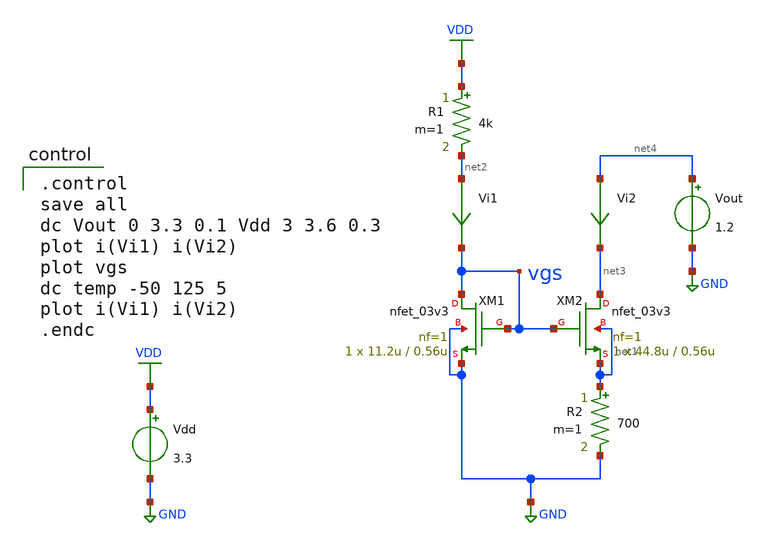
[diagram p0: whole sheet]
** sch_path: current-source/cs-widlar.sch
**.subckt cs-widlar
Vdd VDD GND 3.3
XM1 vgs vgs GND GND nfet_03v3 L=0.56u W=11.2u nf=1 ad='int((nf+1)/2) * W/nf * 0.18u' as='int((nf+2)/2) * W/nf * 0.18u'
+ pd='2*int((nf+1)/2) * (W/nf + 0.18u)' ps='2*int((nf+2)/2) * (W/nf + 0.18u)' nrd='0.18u / W' nrs='0.18u / W'
+ sa=0 sb=0 sd=0 m=1
XM2 net3 vgs net1 net1 nfet_03v3 L=0.56u W=44.8u nf=1 ad='int((nf+1)/2) * W/nf * 0.18u' as='int((nf+2)/2) * W/nf * 0.18u'
+ pd='2*int((nf+1)/2) * (W/nf + 0.18u)' ps='2*int((nf+2)/2) * (W/nf + 0.18u)' nrd='0.18u / W' nrs='0.18u / W'
+ sa=0 sb=0 sd=0 m=1
Vi1 net2 vgs 0
.save i(vi1)
Vi2 net4 net3 0
.save i(vi2)
R1 VDD net2 4k m=1
Vout net4 GND 1.2
R2 net1 GND 700 m=1
**** begin user architecture code

.include $::180MCU_MODELS/design.ngspice
.lib $::180MCU_MODELS/sm141064.ngspice typical
.lib $::180MCU_MODELS/sm141064.ngspice res_typical
.lib $::180MCU_MODELS/sm141064.ngspice moscap_typical
.lib $::180MCU_MODELS/sm141064.ngspice bjt_typical
* .lib $::180MCU_MODELS/sm141064.ngspice res_statistical


.control
save all
dc Vout 0 3.3 0.1 Vdd 3 3.6 0.3
plot i(Vi1) i(Vi2)
plot vgs
dc temp -50 125 5
plot i(Vi1) i(Vi2)
.endc

**** end user architecture code
**.ends
.GLOBAL GND
.GLOBAL VDD
.end
